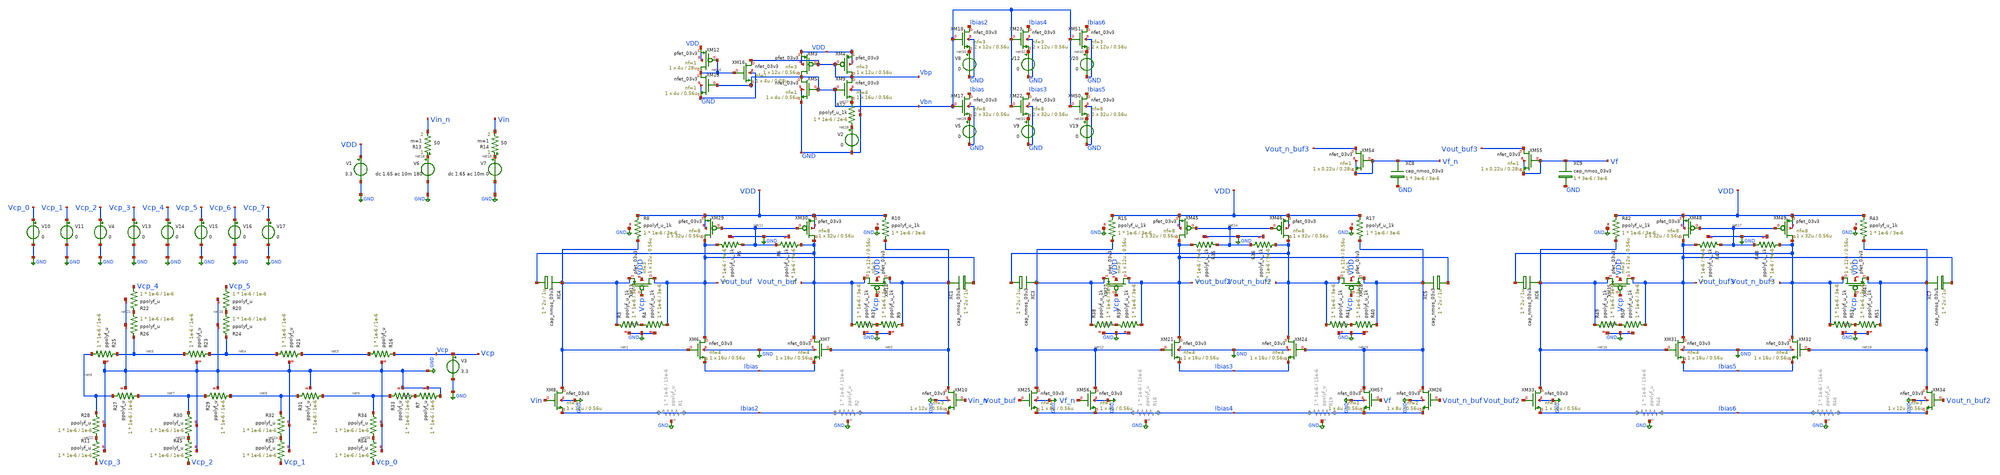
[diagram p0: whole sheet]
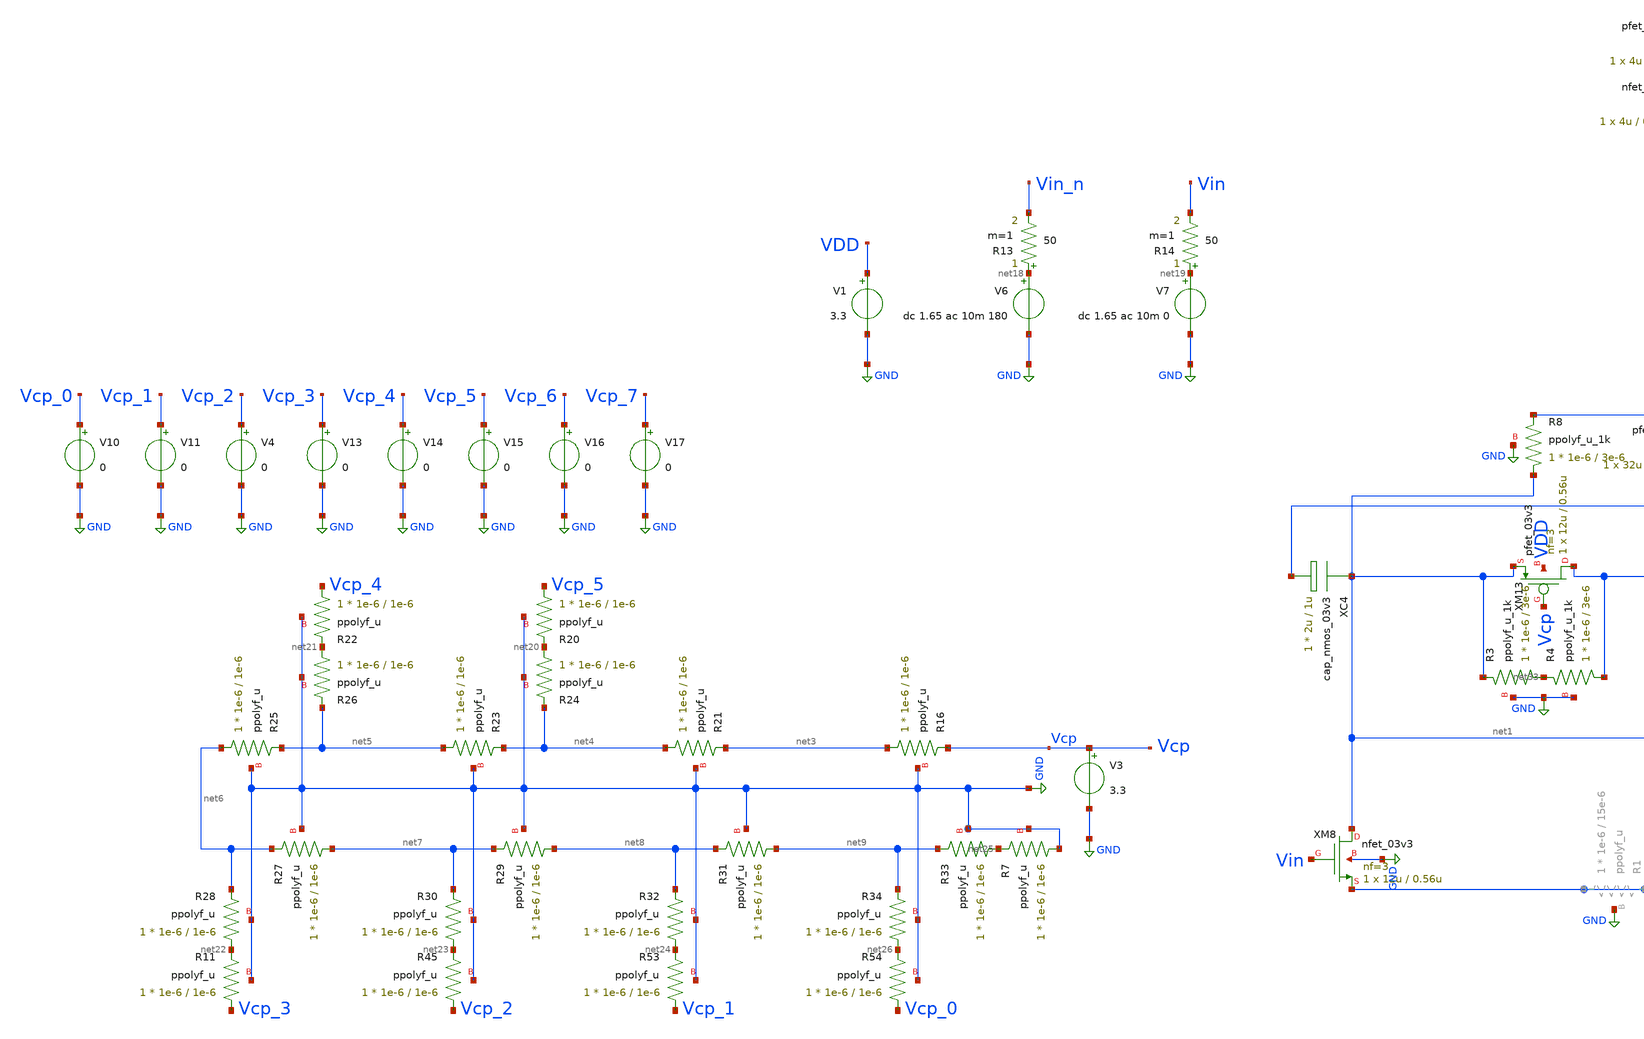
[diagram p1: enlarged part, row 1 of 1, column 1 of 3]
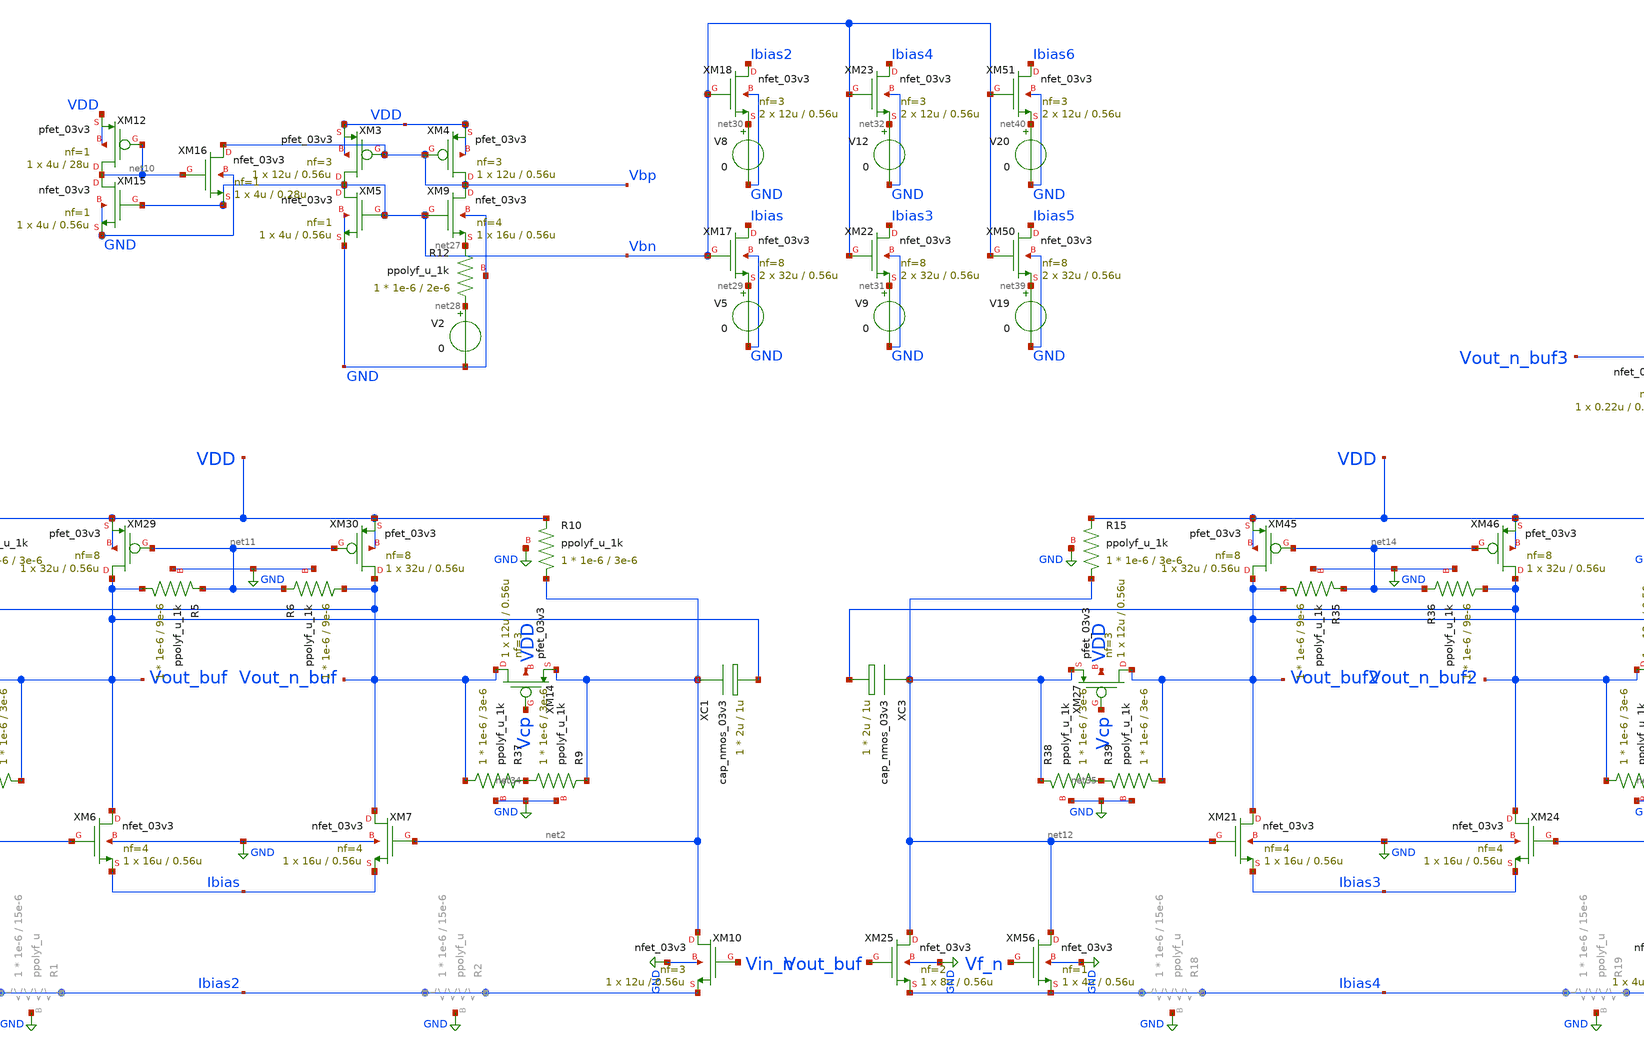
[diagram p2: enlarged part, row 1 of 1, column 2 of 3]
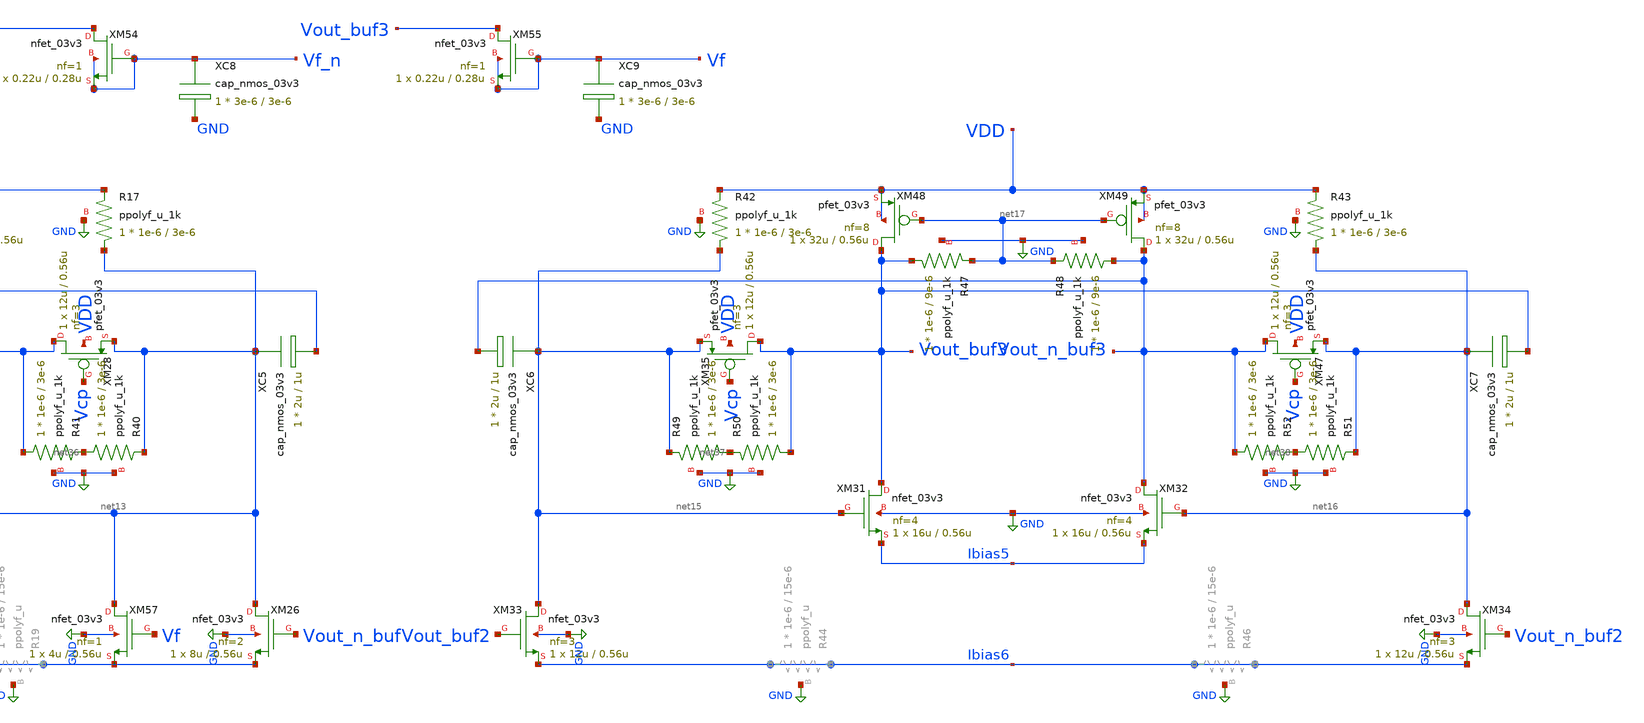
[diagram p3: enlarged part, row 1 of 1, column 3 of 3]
** sch_path: blocks/vga/vga.sch
**.subckt vga
V1 VDD GND 3.3
V6 net18 GND dc 1.65 ac 10m 180
XM6 Vout_buf net1 Ibias GND nfet_03v3 L=0.56u W=16u nf=4 ad='int((nf+1)/2) * W/nf * 0.18u' as='int((nf+2)/2) * W/nf * 0.18u'
+ pd='2*int((nf+1)/2) * (W/nf + 0.18u)' ps='2*int((nf+2)/2) * (W/nf + 0.18u)' nrd='0.18u / W' nrs='0.18u / W'
+ sa=0 sb=0 sd=0 m=1
XM7 Vout_n_buf net2 Ibias GND nfet_03v3 L=0.56u W=16u nf=4 ad='int((nf+1)/2) * W/nf * 0.18u' as='int((nf+2)/2) * W/nf * 0.18u'
+ pd='2*int((nf+1)/2) * (W/nf + 0.18u)' ps='2*int((nf+2)/2) * (W/nf + 0.18u)' nrd='0.18u / W' nrs='0.18u / W'
+ sa=0 sb=0 sd=0 m=1
XM8 net1 Vin Ibias2 GND nfet_03v3 L=0.56u W=12u nf=3 ad='int((nf+1)/2) * W/nf * 0.18u' as='int((nf+2)/2) * W/nf * 0.18u'
+ pd='2*int((nf+1)/2) * (W/nf + 0.18u)' ps='2*int((nf+2)/2) * (W/nf + 0.18u)' nrd='0.18u / W' nrs='0.18u / W'
+ sa=0 sb=0 sd=0 m=1
XM10 net2 Vin_n Ibias2 GND nfet_03v3 L=0.56u W=12u nf=3 ad='int((nf+1)/2) * W/nf * 0.18u' as='int((nf+2)/2) * W/nf * 0.18u'
+ pd='2*int((nf+1)/2) * (W/nf + 0.18u)' ps='2*int((nf+2)/2) * (W/nf + 0.18u)' nrd='0.18u / W' nrs='0.18u / W'
+ sa=0 sb=0 sd=0 m=1
V7 net19 GND dc 1.65 ac 10m 0
R14 net19 Vin 50 m=1
R13 net18 Vin_n 50 m=1
XR16 net3 Vcp GND ppolyf_u r_width=1e-6 r_length=1e-6 m=1
XR21 net4 net3 GND ppolyf_u r_width=1e-6 r_length=1e-6 m=1
XR23 net5 net4 GND ppolyf_u r_width=1e-6 r_length=1e-6 m=1
XR24 net20 net4 GND ppolyf_u r_width=1e-6 r_length=1e-6 m=1
XR25 net6 net5 GND ppolyf_u r_width=1e-6 r_length=1e-6 m=1
XR26 net21 net5 GND ppolyf_u r_width=1e-6 r_length=1e-6 m=1
XR27 net7 net6 GND ppolyf_u r_width=1e-6 r_length=1e-6 m=1
XR28 net22 net6 GND ppolyf_u r_width=1e-6 r_length=1e-6 m=1
XR29 net8 net7 GND ppolyf_u r_width=1e-6 r_length=1e-6 m=1
XR30 net23 net7 GND ppolyf_u r_width=1e-6 r_length=1e-6 m=1
XR31 net9 net8 GND ppolyf_u r_width=1e-6 r_length=1e-6 m=1
XR32 net24 net8 GND ppolyf_u r_width=1e-6 r_length=1e-6 m=1
XR33 net25 net9 GND ppolyf_u r_width=1e-6 r_length=1e-6 m=1
XR34 net26 net9 GND ppolyf_u r_width=1e-6 r_length=1e-6 m=1
V10 Vcp_0 GND 0
V11 Vcp_1 GND 0
V4 Vcp_2 GND 0
V13 Vcp_3 GND 0
V14 Vcp_4 GND 0
V15 Vcp_5 GND 0
V16 Vcp_6 GND 0
V17 Vcp_7 GND 0
V3 Vcp GND 3.3
XM13 Vout_buf Vcp net1 VDD pfet_03v3 L=0.56u W=12u nf=3 ad='int((nf+1)/2) * W/nf * 0.18u' as='int((nf+2)/2) * W/nf * 0.18u'
+ pd='2*int((nf+1)/2) * (W/nf + 0.18u)' ps='2*int((nf+2)/2) * (W/nf + 0.18u)' nrd='0.18u / W' nrs='0.18u / W'
+ sa=0 sb=0 sd=0 m=1
XM14 Vout_n_buf Vcp net2 VDD pfet_03v3 L=0.56u W=12u nf=3 ad='int((nf+1)/2) * W/nf * 0.18u' as='int((nf+2)/2) * W/nf * 0.18u'
+ pd='2*int((nf+1)/2) * (W/nf + 0.18u)' ps='2*int((nf+2)/2) * (W/nf + 0.18u)' nrd='0.18u / W' nrs='0.18u / W'
+ sa=0 sb=0 sd=0 m=1
XR8 net1 VDD GND ppolyf_u_1k r_width=1e-6 r_length=3e-6 m=1
XR10 net2 VDD GND ppolyf_u_1k r_width=1e-6 r_length=3e-6 m=1
XC4 net1 Vout_n_buf cap_nmos_03v3 c_width=2u c_length=1u m=1
XC1 net2 Vout_buf cap_nmos_03v3 c_width=2u c_length=1u m=1
XM3 Vbn Vbp VDD VDD pfet_03v3 L=0.56u W=12u nf=3 ad='int((nf+1)/2) * W/nf * 0.18u' as='int((nf+2)/2) * W/nf * 0.18u'
+ pd='2*int((nf+1)/2) * (W/nf + 0.18u)' ps='2*int((nf+2)/2) * (W/nf + 0.18u)' nrd='0.18u / W' nrs='0.18u / W'
+ sa=0 sb=0 sd=0 m=1
XM4 Vbp Vbp VDD VDD pfet_03v3 L=0.56u W=12u nf=3 ad='int((nf+1)/2) * W/nf * 0.18u' as='int((nf+2)/2) * W/nf * 0.18u'
+ pd='2*int((nf+1)/2) * (W/nf + 0.18u)' ps='2*int((nf+2)/2) * (W/nf + 0.18u)' nrd='0.18u / W' nrs='0.18u / W'
+ sa=0 sb=0 sd=0 m=1
XM5 Vbn Vbn GND GND nfet_03v3 L=0.56u W=4u nf=1 ad='int((nf+1)/2) * W/nf * 0.18u' as='int((nf+2)/2) * W/nf * 0.18u'
+ pd='2*int((nf+1)/2) * (W/nf + 0.18u)' ps='2*int((nf+2)/2) * (W/nf + 0.18u)' nrd='0.18u / W' nrs='0.18u / W'
+ sa=0 sb=0 sd=0 m=1
XM9 Vbp Vbn net27 GND nfet_03v3 L=0.56u W=16u nf=4 ad='int((nf+1)/2) * W/nf * 0.18u' as='int((nf+2)/2) * W/nf * 0.18u'
+ pd='2*int((nf+1)/2) * (W/nf + 0.18u)' ps='2*int((nf+2)/2) * (W/nf + 0.18u)' nrd='0.18u / W' nrs='0.18u / W'
+ sa=0 sb=0 sd=0 m=1
XM12 net10 net10 VDD VDD pfet_03v3 L=28u W=4u nf=1 ad='int((nf+1)/2) * W/nf * 0.18u' as='int((nf+2)/2) * W/nf * 0.18u'
+ pd='2*int((nf+1)/2) * (W/nf + 0.18u)' ps='2*int((nf+2)/2) * (W/nf + 0.18u)' nrd='0.18u / W' nrs='0.18u / W'
+ sa=0 sb=0 sd=0 m=1
XM15 net10 Vbn GND GND nfet_03v3 L=0.56u W=4u nf=1 ad='int((nf+1)/2) * W/nf * 0.18u' as='int((nf+2)/2) * W/nf * 0.18u'
+ pd='2*int((nf+1)/2) * (W/nf + 0.18u)' ps='2*int((nf+2)/2) * (W/nf + 0.18u)' nrd='0.18u / W' nrs='0.18u / W'
+ sa=0 sb=0 sd=0 m=1
XM16 Vbp net10 Vbn GND nfet_03v3 L=0.28u W=4u nf=1 ad='int((nf+1)/2) * W/nf * 0.18u' as='int((nf+2)/2) * W/nf * 0.18u'
+ pd='2*int((nf+1)/2) * (W/nf + 0.18u)' ps='2*int((nf+2)/2) * (W/nf + 0.18u)' nrd='0.18u / W' nrs='0.18u / W'
+ sa=0 sb=0 sd=0 m=1
XR12 net28 net27 GND ppolyf_u_1k r_width=1e-6 r_length=2e-6 m=1
V2 net28 GND 0
XM17 Ibias Vbn net29 GND nfet_03v3 L=0.56u W=32u nf=8 ad='int((nf+1)/2) * W/nf * 0.18u' as='int((nf+2)/2) * W/nf * 0.18u'
+ pd='2*int((nf+1)/2) * (W/nf + 0.18u)' ps='2*int((nf+2)/2) * (W/nf + 0.18u)' nrd='0.18u / W' nrs='0.18u / W'
+ sa=0 sb=0 sd=0 m=2
V5 net29 GND 0
XM18 Ibias2 Vbn net30 GND nfet_03v3 L=0.56u W=12u nf=3 ad='int((nf+1)/2) * W/nf * 0.18u' as='int((nf+2)/2) * W/nf * 0.18u'
+ pd='2*int((nf+1)/2) * (W/nf + 0.18u)' ps='2*int((nf+2)/2) * (W/nf + 0.18u)' nrd='0.18u / W' nrs='0.18u / W'
+ sa=0 sb=0 sd=0 m=2
V8 net30 GND 0
XM22 Ibias3 Vbn net31 GND nfet_03v3 L=0.56u W=32u nf=8 ad='int((nf+1)/2) * W/nf * 0.18u' as='int((nf+2)/2) * W/nf * 0.18u'
+ pd='2*int((nf+1)/2) * (W/nf + 0.18u)' ps='2*int((nf+2)/2) * (W/nf + 0.18u)' nrd='0.18u / W' nrs='0.18u / W'
+ sa=0 sb=0 sd=0 m=2
V9 net31 GND 0
XM23 Ibias4 Vbn net32 GND nfet_03v3 L=0.56u W=12u nf=3 ad='int((nf+1)/2) * W/nf * 0.18u' as='int((nf+2)/2) * W/nf * 0.18u'
+ pd='2*int((nf+1)/2) * (W/nf + 0.18u)' ps='2*int((nf+2)/2) * (W/nf + 0.18u)' nrd='0.18u / W' nrs='0.18u / W'
+ sa=0 sb=0 sd=0 m=2
V12 net32 GND 0
XM29 Vout_buf net11 VDD VDD pfet_03v3 L=0.56u W=32u nf=8 ad='int((nf+1)/2) * W/nf * 0.18u' as='int((nf+2)/2) * W/nf * 0.18u'
+ pd='2*int((nf+1)/2) * (W/nf + 0.18u)' ps='2*int((nf+2)/2) * (W/nf + 0.18u)' nrd='0.18u / W' nrs='0.18u / W'
+ sa=0 sb=0 sd=0 m=1
XM30 Vout_n_buf net11 VDD VDD pfet_03v3 L=0.56u W=32u nf=8 ad='int((nf+1)/2) * W/nf * 0.18u' as='int((nf+2)/2) * W/nf * 0.18u'
+ pd='2*int((nf+1)/2) * (W/nf + 0.18u)' ps='2*int((nf+2)/2) * (W/nf + 0.18u)' nrd='0.18u / W' nrs='0.18u / W'
+ sa=0 sb=0 sd=0 m=1
XR5 Vout_buf net11 GND ppolyf_u_1k r_width=1e-6 r_length=9e-6 m=1
XR6 Vout_n_buf net11 GND ppolyf_u_1k r_width=1e-6 r_length=9e-6 m=1
XR3 net33 net1 GND ppolyf_u_1k r_width=1e-6 r_length=3e-6 m=1
XR4 Vout_buf net33 GND ppolyf_u_1k r_width=1e-6 r_length=3e-6 m=1
XR9 net34 net2 GND ppolyf_u_1k r_width=1e-6 r_length=3e-6 m=1
XR37 Vout_n_buf net34 GND ppolyf_u_1k r_width=1e-6 r_length=3e-6 m=1
XM21 Vout_buf2 net12 Ibias3 GND nfet_03v3 L=0.56u W=16u nf=4 ad='int((nf+1)/2) * W/nf * 0.18u' as='int((nf+2)/2) * W/nf * 0.18u'
+ pd='2*int((nf+1)/2) * (W/nf + 0.18u)' ps='2*int((nf+2)/2) * (W/nf + 0.18u)' nrd='0.18u / W' nrs='0.18u / W'
+ sa=0 sb=0 sd=0 m=1
XM24 Vout_n_buf2 net13 Ibias3 GND nfet_03v3 L=0.56u W=16u nf=4 ad='int((nf+1)/2) * W/nf * 0.18u' as='int((nf+2)/2) * W/nf * 0.18u'
+ pd='2*int((nf+1)/2) * (W/nf + 0.18u)' ps='2*int((nf+2)/2) * (W/nf + 0.18u)' nrd='0.18u / W' nrs='0.18u / W'
+ sa=0 sb=0 sd=0 m=1
XM25 net12 Vout_buf Ibias4 GND nfet_03v3 L=0.56u W=8u nf=2 ad='int((nf+1)/2) * W/nf * 0.18u' as='int((nf+2)/2) * W/nf * 0.18u'
+ pd='2*int((nf+1)/2) * (W/nf + 0.18u)' ps='2*int((nf+2)/2) * (W/nf + 0.18u)' nrd='0.18u / W' nrs='0.18u / W'
+ sa=0 sb=0 sd=0 m=1
XM26 net13 Vout_n_buf Ibias4 GND nfet_03v3 L=0.56u W=8u nf=2 ad='int((nf+1)/2) * W/nf * 0.18u' as='int((nf+2)/2) * W/nf * 0.18u'
+ pd='2*int((nf+1)/2) * (W/nf + 0.18u)' ps='2*int((nf+2)/2) * (W/nf + 0.18u)' nrd='0.18u / W' nrs='0.18u / W'
+ sa=0 sb=0 sd=0 m=1
XM27 Vout_buf2 Vcp net12 VDD pfet_03v3 L=0.56u W=12u nf=3 ad='int((nf+1)/2) * W/nf * 0.18u' as='int((nf+2)/2) * W/nf * 0.18u'
+ pd='2*int((nf+1)/2) * (W/nf + 0.18u)' ps='2*int((nf+2)/2) * (W/nf + 0.18u)' nrd='0.18u / W' nrs='0.18u / W'
+ sa=0 sb=0 sd=0 m=1
XM28 Vout_n_buf2 Vcp net13 VDD pfet_03v3 L=0.56u W=12u nf=3 ad='int((nf+1)/2) * W/nf * 0.18u' as='int((nf+2)/2) * W/nf * 0.18u'
+ pd='2*int((nf+1)/2) * (W/nf + 0.18u)' ps='2*int((nf+2)/2) * (W/nf + 0.18u)' nrd='0.18u / W' nrs='0.18u / W'
+ sa=0 sb=0 sd=0 m=1
XR15 net12 VDD GND ppolyf_u_1k r_width=1e-6 r_length=3e-6 m=1
XR17 net13 VDD GND ppolyf_u_1k r_width=1e-6 r_length=3e-6 m=1
XC3 net12 Vout_n_buf2 cap_nmos_03v3 c_width=2u c_length=1u m=1
XC5 net13 Vout_buf2 cap_nmos_03v3 c_width=2u c_length=1u m=1
XM45 Vout_buf2 net14 VDD VDD pfet_03v3 L=0.56u W=32u nf=8 ad='int((nf+1)/2) * W/nf * 0.18u' as='int((nf+2)/2) * W/nf * 0.18u'
+ pd='2*int((nf+1)/2) * (W/nf + 0.18u)' ps='2*int((nf+2)/2) * (W/nf + 0.18u)' nrd='0.18u / W' nrs='0.18u / W'
+ sa=0 sb=0 sd=0 m=1
XM46 Vout_n_buf2 net14 VDD VDD pfet_03v3 L=0.56u W=32u nf=8 ad='int((nf+1)/2) * W/nf * 0.18u' as='int((nf+2)/2) * W/nf * 0.18u'
+ pd='2*int((nf+1)/2) * (W/nf + 0.18u)' ps='2*int((nf+2)/2) * (W/nf + 0.18u)' nrd='0.18u / W' nrs='0.18u / W'
+ sa=0 sb=0 sd=0 m=1
XR35 Vout_buf2 net14 GND ppolyf_u_1k r_width=1e-6 r_length=9e-6 m=1
XR36 Vout_n_buf2 net14 GND ppolyf_u_1k r_width=1e-6 r_length=9e-6 m=1
XR38 net35 net12 GND ppolyf_u_1k r_width=1e-6 r_length=3e-6 m=1
XR39 Vout_buf2 net35 GND ppolyf_u_1k r_width=1e-6 r_length=3e-6 m=1
XR40 net36 net13 GND ppolyf_u_1k r_width=1e-6 r_length=3e-6 m=1
XR41 Vout_n_buf2 net36 GND ppolyf_u_1k r_width=1e-6 r_length=3e-6 m=1
XM31 Vout_buf3 net15 Ibias5 GND nfet_03v3 L=0.56u W=16u nf=4 ad='int((nf+1)/2) * W/nf * 0.18u' as='int((nf+2)/2) * W/nf * 0.18u'
+ pd='2*int((nf+1)/2) * (W/nf + 0.18u)' ps='2*int((nf+2)/2) * (W/nf + 0.18u)' nrd='0.18u / W' nrs='0.18u / W'
+ sa=0 sb=0 sd=0 m=1
XM32 Vout_n_buf3 net16 Ibias5 GND nfet_03v3 L=0.56u W=16u nf=4 ad='int((nf+1)/2) * W/nf * 0.18u' as='int((nf+2)/2) * W/nf * 0.18u'
+ pd='2*int((nf+1)/2) * (W/nf + 0.18u)' ps='2*int((nf+2)/2) * (W/nf + 0.18u)' nrd='0.18u / W' nrs='0.18u / W'
+ sa=0 sb=0 sd=0 m=1
XM33 net15 Vout_buf2 Ibias6 GND nfet_03v3 L=0.56u W=12u nf=3 ad='int((nf+1)/2) * W/nf * 0.18u' as='int((nf+2)/2) * W/nf * 0.18u'
+ pd='2*int((nf+1)/2) * (W/nf + 0.18u)' ps='2*int((nf+2)/2) * (W/nf + 0.18u)' nrd='0.18u / W' nrs='0.18u / W'
+ sa=0 sb=0 sd=0 m=1
XM34 net16 Vout_n_buf2 Ibias6 GND nfet_03v3 L=0.56u W=12u nf=3 ad='int((nf+1)/2) * W/nf * 0.18u' as='int((nf+2)/2) * W/nf * 0.18u'
+ pd='2*int((nf+1)/2) * (W/nf + 0.18u)' ps='2*int((nf+2)/2) * (W/nf + 0.18u)' nrd='0.18u / W' nrs='0.18u / W'
+ sa=0 sb=0 sd=0 m=1
XM35 Vout_buf3 Vcp net15 VDD pfet_03v3 L=0.56u W=12u nf=3 ad='int((nf+1)/2) * W/nf * 0.18u' as='int((nf+2)/2) * W/nf * 0.18u'
+ pd='2*int((nf+1)/2) * (W/nf + 0.18u)' ps='2*int((nf+2)/2) * (W/nf + 0.18u)' nrd='0.18u / W' nrs='0.18u / W'
+ sa=0 sb=0 sd=0 m=1
XM47 Vout_n_buf3 Vcp net16 VDD pfet_03v3 L=0.56u W=12u nf=3 ad='int((nf+1)/2) * W/nf * 0.18u' as='int((nf+2)/2) * W/nf * 0.18u'
+ pd='2*int((nf+1)/2) * (W/nf + 0.18u)' ps='2*int((nf+2)/2) * (W/nf + 0.18u)' nrd='0.18u / W' nrs='0.18u / W'
+ sa=0 sb=0 sd=0 m=1
XR42 net15 VDD GND ppolyf_u_1k r_width=1e-6 r_length=3e-6 m=1
XR43 net16 VDD GND ppolyf_u_1k r_width=1e-6 r_length=3e-6 m=1
XC6 net15 Vout_n_buf3 cap_nmos_03v3 c_width=2u c_length=1u m=1
XC7 net16 Vout_buf3 cap_nmos_03v3 c_width=2u c_length=1u m=1
XM48 Vout_buf3 net17 VDD VDD pfet_03v3 L=0.56u W=32u nf=8 ad='int((nf+1)/2) * W/nf * 0.18u' as='int((nf+2)/2) * W/nf * 0.18u'
+ pd='2*int((nf+1)/2) * (W/nf + 0.18u)' ps='2*int((nf+2)/2) * (W/nf + 0.18u)' nrd='0.18u / W' nrs='0.18u / W'
+ sa=0 sb=0 sd=0 m=1
XM49 Vout_n_buf3 net17 VDD VDD pfet_03v3 L=0.56u W=32u nf=8 ad='int((nf+1)/2) * W/nf * 0.18u' as='int((nf+2)/2) * W/nf * 0.18u'
+ pd='2*int((nf+1)/2) * (W/nf + 0.18u)' ps='2*int((nf+2)/2) * (W/nf + 0.18u)' nrd='0.18u / W' nrs='0.18u / W'
+ sa=0 sb=0 sd=0 m=1
XR47 Vout_buf3 net17 GND ppolyf_u_1k r_width=1e-6 r_length=9e-6 m=1
XR48 Vout_n_buf3 net17 GND ppolyf_u_1k r_width=1e-6 r_length=9e-6 m=1
XR49 net37 net15 GND ppolyf_u_1k r_width=1e-6 r_length=3e-6 m=1
XR50 Vout_buf3 net37 GND ppolyf_u_1k r_width=1e-6 r_length=3e-6 m=1
XR51 net38 net16 GND ppolyf_u_1k r_width=1e-6 r_length=3e-6 m=1
XR52 Vout_n_buf3 net38 GND ppolyf_u_1k r_width=1e-6 r_length=3e-6 m=1
XM50 Ibias5 Vbn net39 GND nfet_03v3 L=0.56u W=32u nf=8 ad='int((nf+1)/2) * W/nf * 0.18u' as='int((nf+2)/2) * W/nf * 0.18u'
+ pd='2*int((nf+1)/2) * (W/nf + 0.18u)' ps='2*int((nf+2)/2) * (W/nf + 0.18u)' nrd='0.18u / W' nrs='0.18u / W'
+ sa=0 sb=0 sd=0 m=2
V19 net39 GND 0
XM51 Ibias6 Vbn net40 GND nfet_03v3 L=0.56u W=12u nf=3 ad='int((nf+1)/2) * W/nf * 0.18u' as='int((nf+2)/2) * W/nf * 0.18u'
+ pd='2*int((nf+1)/2) * (W/nf + 0.18u)' ps='2*int((nf+2)/2) * (W/nf + 0.18u)' nrd='0.18u / W' nrs='0.18u / W'
+ sa=0 sb=0 sd=0 m=2
V20 net40 GND 0
XM54 Vout_n_buf3 Vf_n Vf_n Vf_n nfet_03v3 L=0.28u W=0.22u nf=1 ad='int((nf+1)/2) * W/nf * 0.18u' as='int((nf+2)/2) * W/nf * 0.18u'
+ pd='2*int((nf+1)/2) * (W/nf + 0.18u)' ps='2*int((nf+2)/2) * (W/nf + 0.18u)' nrd='0.18u / W' nrs='0.18u / W'
+ sa=0 sb=0 sd=0 m=1
XM55 Vout_buf3 Vf Vf Vf nfet_03v3 L=0.28u W=0.22u nf=1 ad='int((nf+1)/2) * W/nf * 0.18u' as='int((nf+2)/2) * W/nf * 0.18u'
+ pd='2*int((nf+1)/2) * (W/nf + 0.18u)' ps='2*int((nf+2)/2) * (W/nf + 0.18u)' nrd='0.18u / W' nrs='0.18u / W'
+ sa=0 sb=0 sd=0 m=1
XM56 net12 Vf_n Ibias4 GND nfet_03v3 L=0.56u W=4u nf=1 ad='int((nf+1)/2) * W/nf * 0.18u' as='int((nf+2)/2) * W/nf * 0.18u'
+ pd='2*int((nf+1)/2) * (W/nf + 0.18u)' ps='2*int((nf+2)/2) * (W/nf + 0.18u)' nrd='0.18u / W' nrs='0.18u / W'
+ sa=0 sb=0 sd=0 m=1
XM57 net13 Vf Ibias4 GND nfet_03v3 L=0.56u W=4u nf=1 ad='int((nf+1)/2) * W/nf * 0.18u' as='int((nf+2)/2) * W/nf * 0.18u'
+ pd='2*int((nf+1)/2) * (W/nf + 0.18u)' ps='2*int((nf+2)/2) * (W/nf + 0.18u)' nrd='0.18u / W' nrs='0.18u / W'
+ sa=0 sb=0 sd=0 m=1
XC8 Vf_n GND cap_nmos_03v3 c_width=3e-6 c_length=3e-6 m=1
XC9 Vf GND cap_nmos_03v3 c_width=3e-6 c_length=3e-6 m=1
XR7 GND net25 GND ppolyf_u r_width=1e-6 r_length=1e-6 m=1
XR11 Vcp_3 net22 GND ppolyf_u r_width=1e-6 r_length=1e-6 m=1
XR45 Vcp_2 net23 GND ppolyf_u r_width=1e-6 r_length=1e-6 m=1
XR53 Vcp_1 net24 GND ppolyf_u r_width=1e-6 r_length=1e-6 m=1
XR54 Vcp_0 net26 GND ppolyf_u r_width=1e-6 r_length=1e-6 m=1
XR20 Vcp_5 net20 GND ppolyf_u r_width=1e-6 r_length=1e-6 m=1
XR22 Vcp_4 net21 GND ppolyf_u r_width=1e-6 r_length=1e-6 m=1
**** begin user architecture code


.include /foss/pdks/gf180mcuD/libs.tech/ngspice/design.ngspice
.lib /foss/pdks/gf180mcuD/libs.tech/ngspice/sm141064.ngspice ff
.lib /foss/pdks/gf180mcuD/libs.tech/ngspice/sm141064.ngspice bjt_ff
.lib /foss/pdks/gf180mcuD/libs.tech/ngspice/sm141064.ngspice diode_ff
.lib /foss/pdks/gf180mcuD/libs.tech/ngspice/sm141064.ngspice res_ff
.lib /foss/pdks/gf180mcuD/libs.tech/ngspice/sm141064.ngspice mimcap_ff
.lib /foss/pdks/gf180mcuD/libs.tech/ngspice/sm141064.ngspice moscap_ff
.option method=gear

.control
set temp = 85
  * 1. Setup the sweep parameters
  let v_ctrl = 3.3

  let f_start = 1
  let f_stop = 3.2G
  let f_points = 120

  * 2. Initialize vectors to store results
  let gain_db = unitvec(f_points)

  alter v3 = v_ctrl
  ac dec $&f_points $&f_start $&f_stop

  * 4. Calculate Differential Gain in dB
  * Formula: 20 * log10(|Vout_diff| / |Vin_diff|)
  let vin_mag = mag(v(vin) - v(vin_n))
  let vout_s_mag = mag(v(vout_buf3))
  let vout_buf_mag = mag(v(vout_buf3) - v(vout_n_buf3))
  let vout_s_gain = 20 * log10(vout_s_mag / vin_mag)
  let vout_buf_gain = 20 * log10(vout_buf_mag / vin_mag)

  * Credit to marcel hendrix
  * https://sourceforge.net/p/ngspice/discussion/133842/thread/2031ad61/
  meas ac peak  MAX  vout_s_mag FROM=$&f_start TO=$&f_stop
  let f3db = peak/sqrt(2)
  meas ac lo_3db WHEN vout_s_mag=f3db RISE=1
  meas ac hi_3db WHEN vout_s_mag=f3db FALL=1

  meas ac peak  MAX  vout_buf_mag FROM=$&f_start TO=$&f_stop
  let f3db = peak/sqrt(2)
  meas ac lo_3db WHEN vout_buf_mag=f3db RISE=1
  meas ac hi_3db WHEN vout_buf_mag=f3db FALL=1

  * 5. Save results to vectors
  plot vout_s_gain vout_buf_gain title 'Gain (dB) vs. Frequency from 1MHz to 3.2GHz, 0.6 vctrl' ylimit
+ -20 60
.endc


**** end user architecture code
**.ends
.GLOBAL GND
.end
